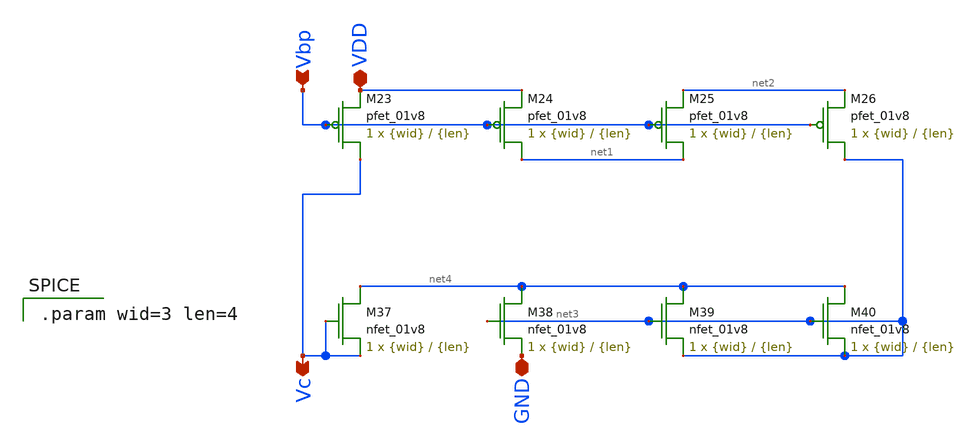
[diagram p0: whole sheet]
** sch_path: mp3/cascode_bias_lds.sch
**.subckt cascode_bias_lds GND Vc VDD Vbp
*.iopin GND
*.opin Vc
*.iopin VDD
*.ipin Vbp
XM23 Vc Vbp VDD VDD sky130_fd_pr__pfet_01v8 L={len} W={wid} nf=1 ad='int((nf+1)/2) * W/nf * 0.29' as='int((nf+2)/2) * W/nf * 0.29'
+ pd='2*int((nf+1)/2) * (W/nf + 0.29)' ps='2*int((nf+2)/2) * (W/nf + 0.29)' nrd='0.29 / W' nrs='0.29 / W'
+ sa=0 sb=0 sd=0 mult=1 m=1
XM24 net1 Vbp VDD VDD sky130_fd_pr__pfet_01v8 L={len} W={wid} nf=1 ad='int((nf+1)/2) * W/nf * 0.29' as='int((nf+2)/2) * W/nf * 0.29'
+ pd='2*int((nf+1)/2) * (W/nf + 0.29)' ps='2*int((nf+2)/2) * (W/nf + 0.29)' nrd='0.29 / W' nrs='0.29 / W'
+ sa=0 sb=0 sd=0 mult=1 m=1
XM25 net1 Vbp net2 VDD sky130_fd_pr__pfet_01v8 L={len} W={wid} nf=1 ad='int((nf+1)/2) * W/nf * 0.29'
+ as='int((nf+2)/2) * W/nf * 0.29' pd='2*int((nf+1)/2) * (W/nf + 0.29)' ps='2*int((nf+2)/2) * (W/nf + 0.29)'
+ nrd='0.29 / W' nrs='0.29 / W' sa=0 sb=0 sd=0 mult=1 m=1
XM26 net3 Vbp net2 VDD sky130_fd_pr__pfet_01v8 L={len} W={wid} nf=1 ad='int((nf+1)/2) * W/nf * 0.29'
+ as='int((nf+2)/2) * W/nf * 0.29' pd='2*int((nf+1)/2) * (W/nf + 0.29)' ps='2*int((nf+2)/2) * (W/nf + 0.29)'
+ nrd='0.29 / W' nrs='0.29 / W' sa=0 sb=0 sd=0 mult=1 m=1
XM37 net4 Vc Vc GND sky130_fd_pr__nfet_01v8 L={len} W={wid} nf=1 ad='int((nf+1)/2) * W/nf * 0.29' as='int((nf+2)/2) * W/nf * 0.29'
+ pd='2*int((nf+1)/2) * (W/nf + 0.29)' ps='2*int((nf+2)/2) * (W/nf + 0.29)' nrd='0.29 / W' nrs='0.29 / W'
+ sa=0 sb=0 sd=0 mult=1 m=1
XM38 net4 net3 GND GND sky130_fd_pr__nfet_01v8 L={len} W={wid} nf=1 ad='int((nf+1)/2) * W/nf * 0.29'
+ as='int((nf+2)/2) * W/nf * 0.29' pd='2*int((nf+1)/2) * (W/nf + 0.29)' ps='2*int((nf+2)/2) * (W/nf + 0.29)'
+ nrd='0.29 / W' nrs='0.29 / W' sa=0 sb=0 sd=0 mult=1 m=1
XM39 net4 net3 net3 GND sky130_fd_pr__nfet_01v8 L={len} W={wid} nf=1 ad='int((nf+1)/2) * W/nf * 0.29'
+ as='int((nf+2)/2) * W/nf * 0.29' pd='2*int((nf+1)/2) * (W/nf + 0.29)' ps='2*int((nf+2)/2) * (W/nf + 0.29)'
+ nrd='0.29 / W' nrs='0.29 / W' sa=0 sb=0 sd=0 mult=1 m=1
XM40 net4 net3 net3 GND sky130_fd_pr__nfet_01v8 L={len} W={wid} nf=1 ad='int((nf+1)/2) * W/nf * 0.29'
+ as='int((nf+2)/2) * W/nf * 0.29' pd='2*int((nf+1)/2) * (W/nf + 0.29)' ps='2*int((nf+2)/2) * (W/nf + 0.29)'
+ nrd='0.29 / W' nrs='0.29 / W' sa=0 sb=0 sd=0 mult=1 m=1
**** begin user architecture code

.param wid=3 len=4

**** end user architecture code
**.ends
.end
